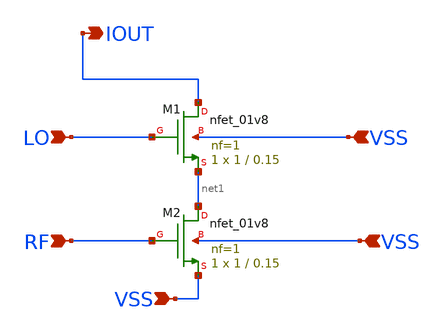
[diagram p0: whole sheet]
** sch_path: mixer.sch
**.subckt mixer LO RF RF VSS IOUT VSS VSS
*.ipin LO
*.ipin RF
*.ipin RF
*.ipin VSS
*.opin IOUT
*.ipin VSS
*.ipin VSS
XM1 IOUT LO net1 VSS sky130_fd_pr__nfet_01v8 L=0.15 W=1 nf=1 ad='int((nf+1)/2) * W/nf * 0.29' as='int((nf+2)/2) * W/nf * 0.29'
+ pd='2*int((nf+1)/2) * (W/nf + 0.29)' ps='2*int((nf+2)/2) * (W/nf + 0.29)' nrd='0.29 / W' nrs='0.29 / W'
+ sa=0 sb=0 sd=0 mult=1 m=1
XM2 net1 RF VSS VSS sky130_fd_pr__nfet_01v8 L=0.15 W=1 nf=1 ad='int((nf+1)/2) * W/nf * 0.29' as='int((nf+2)/2) * W/nf * 0.29'
+ pd='2*int((nf+1)/2) * (W/nf + 0.29)' ps='2*int((nf+2)/2) * (W/nf + 0.29)' nrd='0.29 / W' nrs='0.29 / W'
+ sa=0 sb=0 sd=0 mult=1 m=1
**.ends
.end
